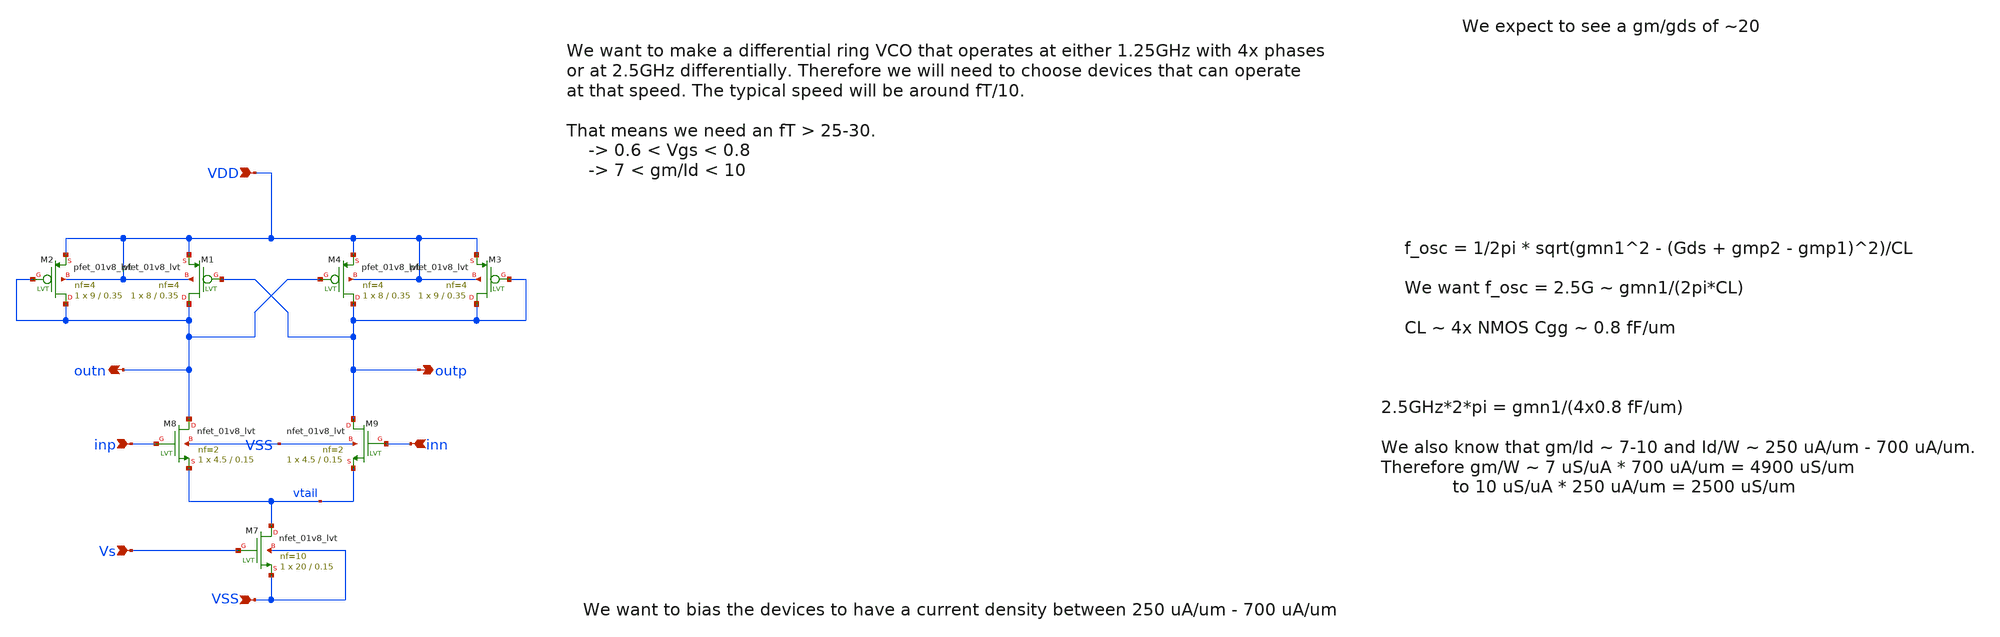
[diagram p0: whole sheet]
** sch_path: src/delay_cell_v1.sch
**.subckt delay_cell_v1 inp inn outp outn VDD VSS Vs
*.ipin inp
*.ipin inn
*.opin outp
*.opin outn
*.ipin VDD
*.ipin VSS
*.ipin Vs
XM8 outn inp vtail VSS sky130_fd_pr__nfet_01v8_lvt L=0.15 W=4.5 nf=2 ad='int((2 + 1)/2) * 4.5 / 2 * 0.29'
+ as='int((2 + 2)/2) * 4.5 / 2 * 0.29' pd='2*int((2 + 1)/2) * (4.5 / 2 + 0.29)' ps='2*int((2 + 2)/2) * (4.5 / 2 + 0.29)'
+ nrd='0.29 / 4.5 ' nrs='0.29 / 4.5 ' sa=0 sb=0 sd=0 mult=1 m=1
XM9 outp inn vtail VSS sky130_fd_pr__nfet_01v8_lvt L=0.15 W=4.5 nf=2 ad='int((2 + 1)/2) * 4.5 / 2 * 0.29'
+ as='int((2 + 2)/2) * 4.5 / 2 * 0.29' pd='2*int((2 + 1)/2) * (4.5 / 2 + 0.29)' ps='2*int((2 + 2)/2) * (4.5 / 2 + 0.29)'
+ nrd='0.29 / 4.5 ' nrs='0.29 / 4.5 ' sa=0 sb=0 sd=0 mult=1 m=1
XM7 vtail Vs VSS VSS sky130_fd_pr__nfet_01v8_lvt L=0.15 W=20 nf=10 ad='int((10 + 1)/2) * 20 / 10 * 0.29'
+ as='int((10 + 2)/2) * 20 / 10 * 0.29' pd='2*int((10 + 1)/2) * (20 / 10 + 0.29)' ps='2*int((10 + 2)/2) * (20 / 10 + 0.29)'
+ nrd='0.29 / 20 ' nrs='0.29 / 20 ' sa=0 sb=0 sd=0 mult=1 m=1
XM3 outp outp VDD VDD sky130_fd_pr__pfet_01v8_lvt L=0.35 W=9 nf=4 ad='int((4 + 1)/2) * 9 / 4 * 0.29'
+ as='int((4 + 2)/2) * 9 / 4 * 0.29' pd='2*int((4 + 1)/2) * (9 / 4 + 0.29)' ps='2*int((4 + 2)/2) * (9 / 4 + 0.29)'
+ nrd='0.29 / 9 ' nrs='0.29 / 9 ' sa=0 sb=0 sd=0 mult=1 m=1
XM2 outn outn VDD VDD sky130_fd_pr__pfet_01v8_lvt L=0.35 W=9 nf=4 ad='int((4 + 1)/2) * 9 / 4 * 0.29'
+ as='int((4 + 2)/2) * 9 / 4 * 0.29' pd='2*int((4 + 1)/2) * (9 / 4 + 0.29)' ps='2*int((4 + 2)/2) * (9 / 4 + 0.29)'
+ nrd='0.29 / 9 ' nrs='0.29 / 9 ' sa=0 sb=0 sd=0 mult=1 m=1
XM1 outn outp VDD VDD sky130_fd_pr__pfet_01v8_lvt L=0.35 W=8 nf=4 ad='int((4 + 1)/2) * 8 / 4 * 0.29'
+ as='int((4 + 2)/2) * 8 / 4 * 0.29' pd='2*int((4 + 1)/2) * (8 / 4 + 0.29)' ps='2*int((4 + 2)/2) * (8 / 4 + 0.29)'
+ nrd='0.29 / 8 ' nrs='0.29 / 8 ' sa=0 sb=0 sd=0 mult=1 m=1
XM4 outp outn VDD VDD sky130_fd_pr__pfet_01v8_lvt L=0.35 W=8 nf=4 ad='int((4 + 1)/2) * 8 / 4 * 0.29'
+ as='int((4 + 2)/2) * 8 / 4 * 0.29' pd='2*int((4 + 1)/2) * (8 / 4 + 0.29)' ps='2*int((4 + 2)/2) * (8 / 4 + 0.29)'
+ nrd='0.29 / 8 ' nrs='0.29 / 8 ' sa=0 sb=0 sd=0 mult=1 m=1
**.ends
.end
